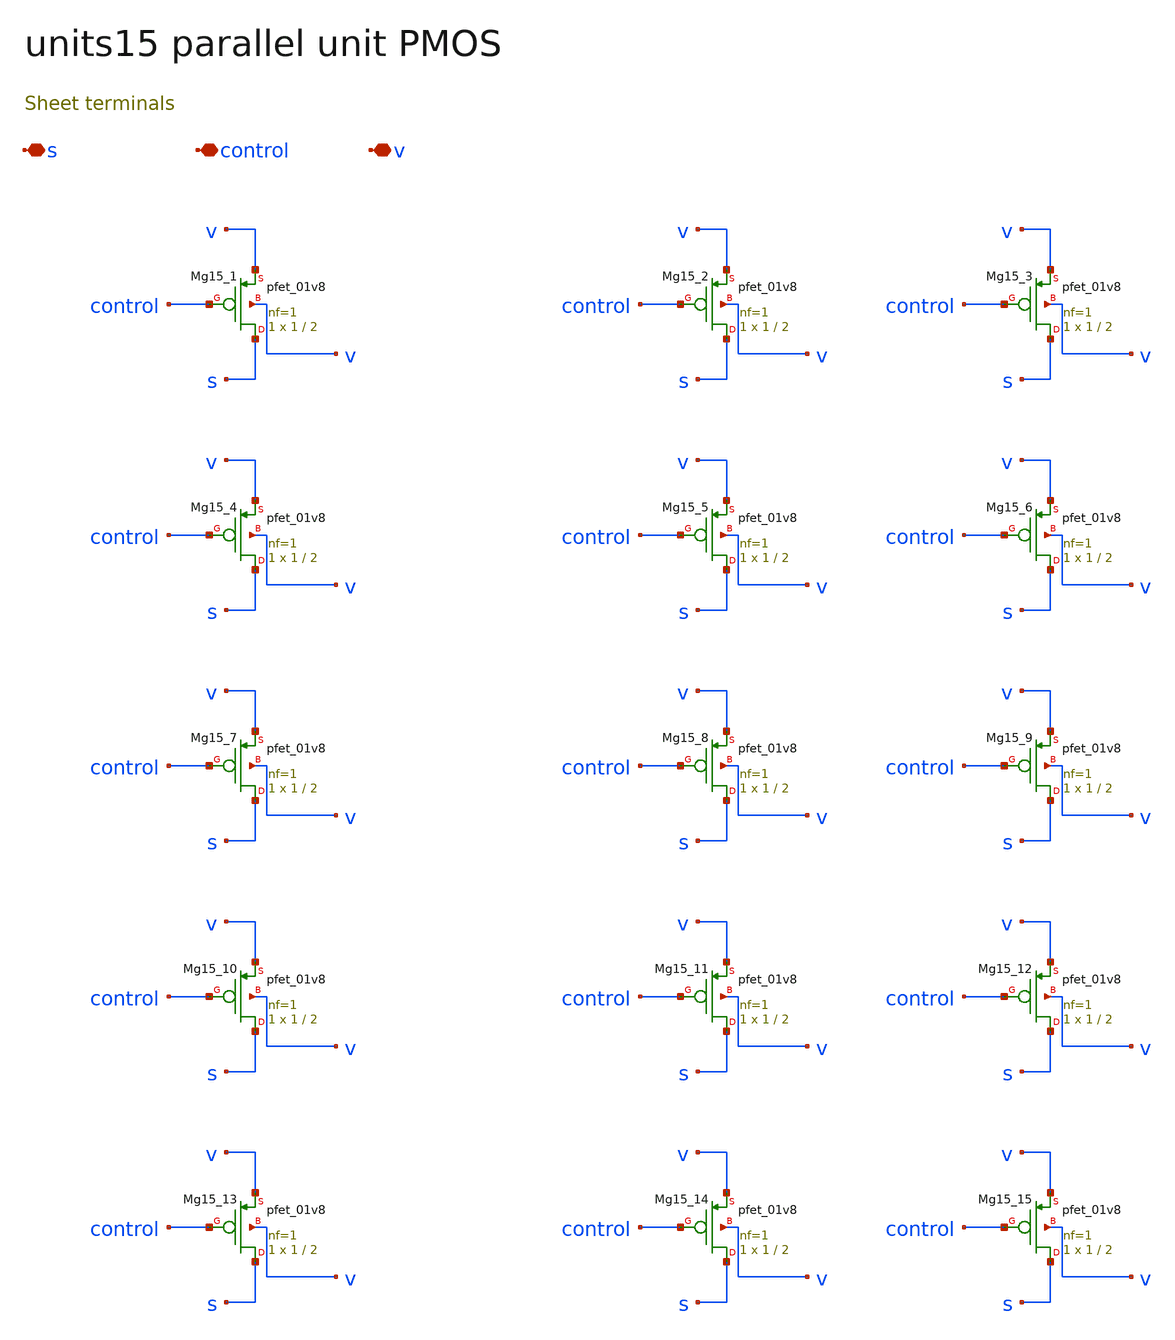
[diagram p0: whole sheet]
** sch_path: review/xschem/units15.sch
**.subckt units15 s control v
*.iopin s
*.iopin control
*.iopin v
XMg15_1 s control v v sky130_fd_pr__pfet_01v8 L=2 W=1 nf=1 ad='int((nf+1)/2) * W/nf * 0.29' as='int((nf+2)/2) * W/nf * 0.29'
+ pd='2*int((nf+1)/2) * (W/nf + 0.29)' ps='2*int((nf+2)/2) * (W/nf + 0.29)' nrd='0.29 / W' nrs='0.29 / W'
+ sa=0 sb=0 sd=0 mult=1 m=1
XMg15_2 s control v v sky130_fd_pr__pfet_01v8 L=2 W=1 nf=1 ad='int((nf+1)/2) * W/nf * 0.29' as='int((nf+2)/2) * W/nf * 0.29'
+ pd='2*int((nf+1)/2) * (W/nf + 0.29)' ps='2*int((nf+2)/2) * (W/nf + 0.29)' nrd='0.29 / W' nrs='0.29 / W'
+ sa=0 sb=0 sd=0 mult=1 m=1
XMg15_3 s control v v sky130_fd_pr__pfet_01v8 L=2 W=1 nf=1 ad='int((nf+1)/2) * W/nf * 0.29' as='int((nf+2)/2) * W/nf * 0.29'
+ pd='2*int((nf+1)/2) * (W/nf + 0.29)' ps='2*int((nf+2)/2) * (W/nf + 0.29)' nrd='0.29 / W' nrs='0.29 / W'
+ sa=0 sb=0 sd=0 mult=1 m=1
XMg15_4 s control v v sky130_fd_pr__pfet_01v8 L=2 W=1 nf=1 ad='int((nf+1)/2) * W/nf * 0.29' as='int((nf+2)/2) * W/nf * 0.29'
+ pd='2*int((nf+1)/2) * (W/nf + 0.29)' ps='2*int((nf+2)/2) * (W/nf + 0.29)' nrd='0.29 / W' nrs='0.29 / W'
+ sa=0 sb=0 sd=0 mult=1 m=1
XMg15_5 s control v v sky130_fd_pr__pfet_01v8 L=2 W=1 nf=1 ad='int((nf+1)/2) * W/nf * 0.29' as='int((nf+2)/2) * W/nf * 0.29'
+ pd='2*int((nf+1)/2) * (W/nf + 0.29)' ps='2*int((nf+2)/2) * (W/nf + 0.29)' nrd='0.29 / W' nrs='0.29 / W'
+ sa=0 sb=0 sd=0 mult=1 m=1
XMg15_6 s control v v sky130_fd_pr__pfet_01v8 L=2 W=1 nf=1 ad='int((nf+1)/2) * W/nf * 0.29' as='int((nf+2)/2) * W/nf * 0.29'
+ pd='2*int((nf+1)/2) * (W/nf + 0.29)' ps='2*int((nf+2)/2) * (W/nf + 0.29)' nrd='0.29 / W' nrs='0.29 / W'
+ sa=0 sb=0 sd=0 mult=1 m=1
XMg15_7 s control v v sky130_fd_pr__pfet_01v8 L=2 W=1 nf=1 ad='int((nf+1)/2) * W/nf * 0.29' as='int((nf+2)/2) * W/nf * 0.29'
+ pd='2*int((nf+1)/2) * (W/nf + 0.29)' ps='2*int((nf+2)/2) * (W/nf + 0.29)' nrd='0.29 / W' nrs='0.29 / W'
+ sa=0 sb=0 sd=0 mult=1 m=1
XMg15_8 s control v v sky130_fd_pr__pfet_01v8 L=2 W=1 nf=1 ad='int((nf+1)/2) * W/nf * 0.29' as='int((nf+2)/2) * W/nf * 0.29'
+ pd='2*int((nf+1)/2) * (W/nf + 0.29)' ps='2*int((nf+2)/2) * (W/nf + 0.29)' nrd='0.29 / W' nrs='0.29 / W'
+ sa=0 sb=0 sd=0 mult=1 m=1
XMg15_9 s control v v sky130_fd_pr__pfet_01v8 L=2 W=1 nf=1 ad='int((nf+1)/2) * W/nf * 0.29' as='int((nf+2)/2) * W/nf * 0.29'
+ pd='2*int((nf+1)/2) * (W/nf + 0.29)' ps='2*int((nf+2)/2) * (W/nf + 0.29)' nrd='0.29 / W' nrs='0.29 / W'
+ sa=0 sb=0 sd=0 mult=1 m=1
XMg15_10 s control v v sky130_fd_pr__pfet_01v8 L=2 W=1 nf=1 ad='int((nf+1)/2) * W/nf * 0.29' as='int((nf+2)/2) * W/nf * 0.29'
+ pd='2*int((nf+1)/2) * (W/nf + 0.29)' ps='2*int((nf+2)/2) * (W/nf + 0.29)' nrd='0.29 / W' nrs='0.29 / W'
+ sa=0 sb=0 sd=0 mult=1 m=1
XMg15_11 s control v v sky130_fd_pr__pfet_01v8 L=2 W=1 nf=1 ad='int((nf+1)/2) * W/nf * 0.29' as='int((nf+2)/2) * W/nf * 0.29'
+ pd='2*int((nf+1)/2) * (W/nf + 0.29)' ps='2*int((nf+2)/2) * (W/nf + 0.29)' nrd='0.29 / W' nrs='0.29 / W'
+ sa=0 sb=0 sd=0 mult=1 m=1
XMg15_12 s control v v sky130_fd_pr__pfet_01v8 L=2 W=1 nf=1 ad='int((nf+1)/2) * W/nf * 0.29' as='int((nf+2)/2) * W/nf * 0.29'
+ pd='2*int((nf+1)/2) * (W/nf + 0.29)' ps='2*int((nf+2)/2) * (W/nf + 0.29)' nrd='0.29 / W' nrs='0.29 / W'
+ sa=0 sb=0 sd=0 mult=1 m=1
XMg15_13 s control v v sky130_fd_pr__pfet_01v8 L=2 W=1 nf=1 ad='int((nf+1)/2) * W/nf * 0.29' as='int((nf+2)/2) * W/nf * 0.29'
+ pd='2*int((nf+1)/2) * (W/nf + 0.29)' ps='2*int((nf+2)/2) * (W/nf + 0.29)' nrd='0.29 / W' nrs='0.29 / W'
+ sa=0 sb=0 sd=0 mult=1 m=1
XMg15_14 s control v v sky130_fd_pr__pfet_01v8 L=2 W=1 nf=1 ad='int((nf+1)/2) * W/nf * 0.29' as='int((nf+2)/2) * W/nf * 0.29'
+ pd='2*int((nf+1)/2) * (W/nf + 0.29)' ps='2*int((nf+2)/2) * (W/nf + 0.29)' nrd='0.29 / W' nrs='0.29 / W'
+ sa=0 sb=0 sd=0 mult=1 m=1
XMg15_15 s control v v sky130_fd_pr__pfet_01v8 L=2 W=1 nf=1 ad='int((nf+1)/2) * W/nf * 0.29' as='int((nf+2)/2) * W/nf * 0.29'
+ pd='2*int((nf+1)/2) * (W/nf + 0.29)' ps='2*int((nf+2)/2) * (W/nf + 0.29)' nrd='0.29 / W' nrs='0.29 / W'
+ sa=0 sb=0 sd=0 mult=1 m=1
**.ends
.end
